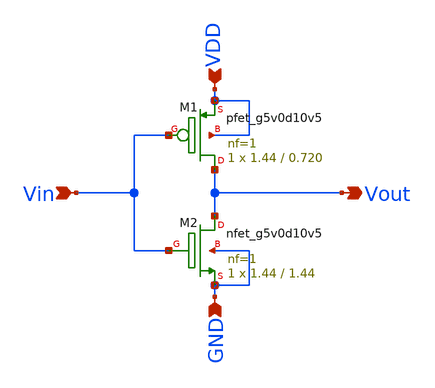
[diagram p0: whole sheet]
** sch_path: xschem/Inverter.sch
**.subckt Inverter Vout Vin VDD GND
*.opin Vout
*.ipin Vin
*.ipin VDD
*.ipin GND
XM1 Vout Vin VDD VDD sky130_fd_pr__pfet_g5v0d10v5 L=0.720 W=1.44 nf=1 ad='int((1 + 1)/2) * 1.44 / 1 * 0.29'
+ as='int((1 + 2)/2) * 1.44 / 1 * 0.29' pd='2*int((1 + 1)/2) * (1.44 / 1 + 0.29)' ps='2*int((1 + 2)/2) * (1.44 / 1 + 0.29)'
+ nrd='0.29 / 1.44 ' nrs='0.29 / 1.44 ' sa=0 sb=0 sd=0 mult=1 m=1
XM2 Vout Vin GND GND sky130_fd_pr__nfet_g5v0d10v5 L=1.44 W=1.44 nf=1 ad='int((1 + 1)/2) * 1.44 / 1 * 0.29'
+ as='int((1 + 2)/2) * 1.44 / 1 * 0.29' pd='2*int((1 + 1)/2) * (1.44 / 1 + 0.29)' ps='2*int((1 + 2)/2) * (1.44 / 1 + 0.29)'
+ nrd='0.29 / 1.44 ' nrs='0.29 / 1.44 ' sa=0 sb=0 sd=0 mult=1 m=1
**.ends
.end
